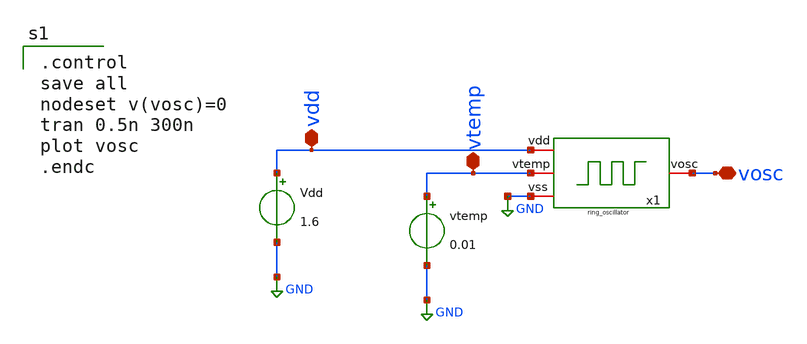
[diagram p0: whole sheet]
** sch_path: XSCHEM/ring_oscillator_tb.sch
**.subckt ring_oscillator_tb vosc vdd vtemp
*.iopin vosc
*.iopin vdd
*.iopin vtemp
Vdd vdd GND 1.6
vtemp vtemp GND 0.01
x1 vdd vosc GND vtemp ring_oscillator
**** begin user architecture code

.control
save all
nodeset v(vosc)=0
tran 0.5n 300n
plot vosc
.endc


** opencircuitdesign pdks install
.lib $::SKYWATER_MODELS/sky130.lib.spice ff
.include /usr/local/share/pdk/sky130A/libs.ref/sky130_fd_sc_hd/spice/sky130_fd_sc_hd.spice

**** end user architecture code
**.ends

* expanding   symbol:  Documentos/TESIS DE GRADO/WORK_IN_PROGRESS/My_xschem/ring_oscillator.sym # of
*+ pins=4
** sym_path: XSCHEM/ring_oscillator.sym
** sch_path: XSCHEM/ring_oscillator.sch
.subckt ring_oscillator vdd vosc vss vtemp
*.iopin vtemp
*.iopin vss
*.iopin vdd
*.iopin vosc
XM7 net1 vosc vdd vdd sky130_fd_pr__pfet_01v8_lvt L=2 W=12 nf=1 ad='int((nf+1)/2) * W/nf * 0.29' as='int((nf+2)/2) * W/nf * 0.29'
+ pd='2*int((nf+1)/2) * (W/nf + 0.29)' ps='2*int((nf+2)/2) * (W/nf + 0.29)' nrd='0.29 / W' nrs='0.29 / W'
+ sa=0 sb=0 sd=0 mult=1 m=1
XM8 net1 vosc vss vss sky130_fd_pr__nfet_01v8_lvt L=2 W=4 nf=1 ad='int((nf+1)/2) * W/nf * 0.29' as='int((nf+2)/2) * W/nf * 0.29'
+ pd='2*int((nf+1)/2) * (W/nf + 0.29)' ps='2*int((nf+2)/2) * (W/nf + 0.29)' nrd='0.29 / W' nrs='0.29 / W'
+ sa=0 sb=0 sd=0 mult=1 m=1
XM9 net2 net1 vdd vdd sky130_fd_pr__pfet_01v8_lvt L=2 W=12 nf=1 ad='int((nf+1)/2) * W/nf * 0.29' as='int((nf+2)/2) * W/nf * 0.29'
+ pd='2*int((nf+1)/2) * (W/nf + 0.29)' ps='2*int((nf+2)/2) * (W/nf + 0.29)' nrd='0.29 / W' nrs='0.29 / W'
+ sa=0 sb=0 sd=0 mult=1 m=1
XM10 net2 net1 vss vss sky130_fd_pr__nfet_01v8_lvt L=2 W=4 nf=1 ad='int((nf+1)/2) * W/nf * 0.29' as='int((nf+2)/2) * W/nf * 0.29'
+ pd='2*int((nf+1)/2) * (W/nf + 0.29)' ps='2*int((nf+2)/2) * (W/nf + 0.29)' nrd='0.29 / W' nrs='0.29 / W'
+ sa=0 sb=0 sd=0 mult=1 m=1
XM11 vosc net2 vdd vdd sky130_fd_pr__pfet_01v8_lvt L=2 W=12 nf=1 ad='int((nf+1)/2) * W/nf * 0.29' as='int((nf+2)/2) * W/nf * 0.29'
+ pd='2*int((nf+1)/2) * (W/nf + 0.29)' ps='2*int((nf+2)/2) * (W/nf + 0.29)' nrd='0.29 / W' nrs='0.29 / W'
+ sa=0 sb=0 sd=0 mult=1 m=1
XM12 vosc net2 vss vss sky130_fd_pr__nfet_01v8_lvt L=2 W=4 nf=1 ad='int((nf+1)/2) * W/nf * 0.29' as='int((nf+2)/2) * W/nf * 0.29'
+ pd='2*int((nf+1)/2) * (W/nf + 0.29)' ps='2*int((nf+2)/2) * (W/nf + 0.29)' nrd='0.29 / W' nrs='0.29 / W'
+ sa=0 sb=0 sd=0 mult=1 m=1
XC1 vosc vtemp vss sky130_fd_pr__cap_var_lvt W=5 L=5 VM=1 m=1
XC2 net2 vtemp vss sky130_fd_pr__cap_var_lvt W=5 L=5 VM=1 m=1
XC3 net1 vtemp vss sky130_fd_pr__cap_var_lvt W=5 L=5 VM=1 m=1
.ends

.GLOBAL GND
.end
